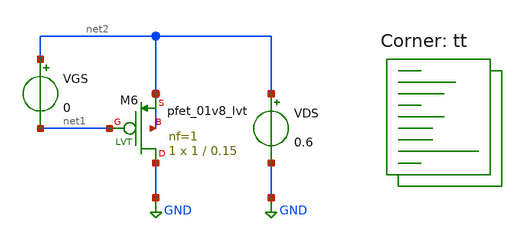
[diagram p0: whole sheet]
** sch_path: pll/lc_vco_lib_Ahmed_Elshahat/CMOS_LC_VCO/PMOS_charts/spice_files/PMOS_char.sch
**.subckt PMOS_char
VDS net2 GND 0.6
VGS net2 net1 0
XM6 GND net1 net2 net2 sky130_fd_pr__pfet_01v8_lvt L=0.15 W=1 nf=1 ad='int((1 + 1)/2) * 1 / 1 * 0.29'
+ as='int((1 + 2)/2) * 1 / 1 * 0.29' pd='2*int((1 + 1)/2) * (1 / 1 + 0.29)' ps='2*int((1 + 2)/2) * (1 / 1 + 0.29)'
+ nrd='0.29 / 1 ' nrs='0.29 / 1 ' sa=0 sb=0 sd=0 mult=1 m=1
**** begin user architecture code
.lib $::SKYWATER_MODELS/sky130.lib.spice tt
**** end user architecture code
**.ends
.GLOBAL GND
.end
